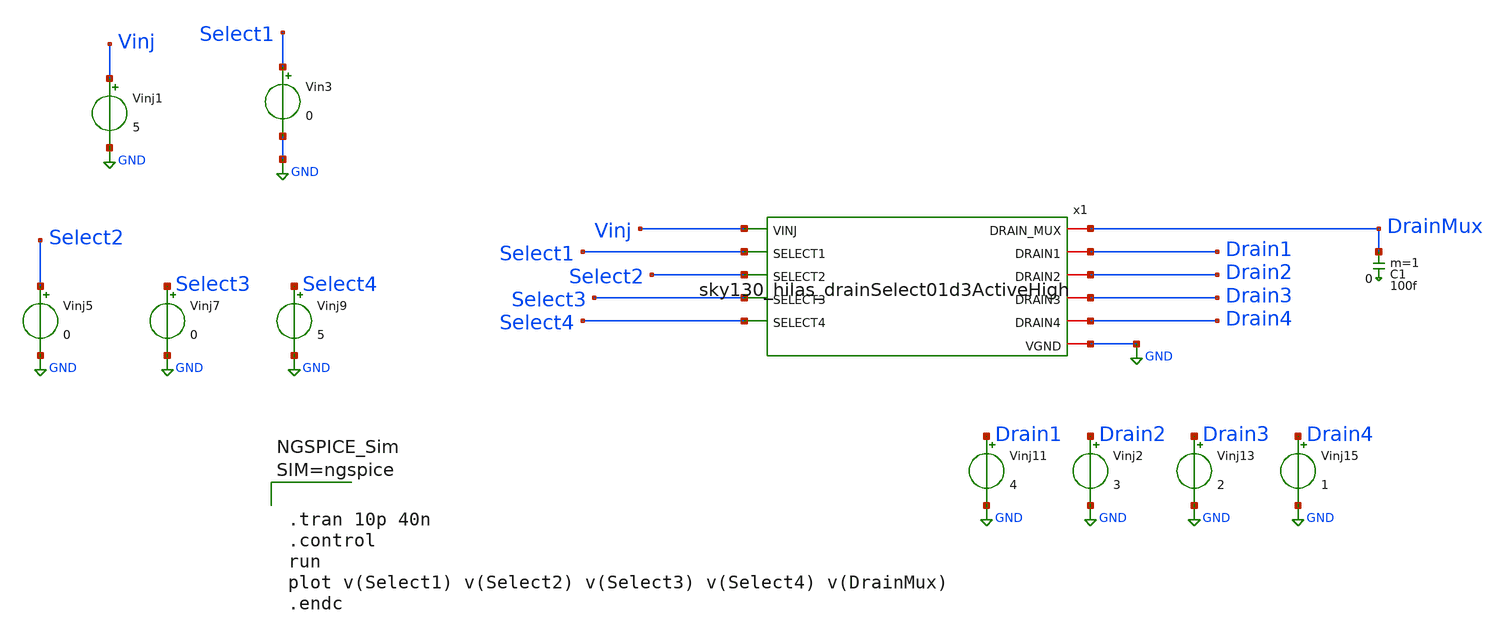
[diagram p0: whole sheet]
** sch_path: sky130_cells/Practice/DrainSelect/drainSelectActiveHighTB.sch
**.subckt drainSelectActiveHighTB
Vinj1 Vinj GND 5
Vin3 Select1 GND 0
Vinj5 Select2 GND 0
Vinj7 Select3 GND 0
Vinj9 Select4 GND 5
Vinj11 Drain1 GND 4
x1 Vinj DrainMux Select1 Drain1 Select2 Drain2 Select3 Drain3 Select4 Drain4 GND
+ sky130_hilas_drainSelect01d3ActiveHigh
C1 DrainMux 0 100f m=1
Vinj2 Drain2 GND 3
Vinj13 Drain3 GND 2
Vinj15 Drain4 GND 1
**** begin user architecture code
 .lib /usr/local/share/pdk/sky130A/libs.tech/ngspice/sky130.lib.spice tt



.tran 10p 40n
.control
run
plot v(Select1) v(Select2) v(Select3) v(Select4) v(DrainMux)
.endc



**** end user architecture code
**.ends

* expanding   symbol:  sky130_cells/Practice/DrainSelect/sky130_hilas_drainSelect01d3ActiveHigh.sym
*+ # of pins=11
** sym_path: sky130_cells/Practice/DrainSelect/sky130_hilas_drainSelect01d3ActiveHigh.sym
** sch_path: sky130_cells/Practice/DrainSelect/sky130_hilas_drainSelect01d3ActiveHigh.sch
.subckt sky130_hilas_drainSelect01d3ActiveHigh VINJ DRAIN_MUX SELECT1 DRAIN1 SELECT2 DRAIN2 SELECT3
+ DRAIN3 SELECT4 DRAIN4 VGND
*.ipin SELECT1
*.iopin DRAIN_MUX
*.iopin DRAIN1
*.ipin VINJ
*.ipin SELECT2
*.iopin DRAIN2
*.ipin SELECT3
*.iopin DRAIN3
*.ipin SELECT4
*.iopin DRAIN4
*.iopin VGND
XM15 net1 SELECT1 VGND VGND sky130_fd_pr__nfet_g5v0d10v5 L=0.5 W=1 nf=1 ad='int((nf+1)/2) * W/nf * 0.29'
+ as='int((nf+2)/2) * W/nf * 0.29' pd='2*int((nf+1)/2) * (W/nf + 0.29)' ps='2*int((nf+2)/2) * (W/nf + 0.29)'
+ nrd='0.29 / W' nrs='0.29 / W' sa=0 sb=0 sd=0 mult=1 m=1
XM17 DRAIN1 net1 DRAIN_MUX VINJ sky130_fd_pr__pfet_g5v0d10v5 L=0.5 W=1 nf=1 ad='int((nf+1)/2) * W/nf * 0.29'
+ as='int((nf+2)/2) * W/nf * 0.29' pd='2*int((nf+1)/2) * (W/nf + 0.29)' ps='2*int((nf+2)/2) * (W/nf + 0.29)'
+ nrd='0.29 / W' nrs='0.29 / W' sa=0 sb=0 sd=0 mult=1 m=1
XM30 VINJ SELECT1 DRAIN1 VINJ sky130_fd_pr__pfet_g5v0d10v5 L=0.5 W=1 nf=1 ad='int((nf+1)/2) * W/nf * 0.29'
+ as='int((nf+2)/2) * W/nf * 0.29' pd='2*int((nf+1)/2) * (W/nf + 0.29)' ps='2*int((nf+2)/2) * (W/nf + 0.29)'
+ nrd='0.29 / W' nrs='0.29 / W' sa=0 sb=0 sd=0 mult=1 m=1
XM31 net1 SELECT1 VINJ VINJ sky130_fd_pr__pfet_g5v0d10v5 L=0.5 W=1 nf=1 ad='int((nf+1)/2) * W/nf * 0.29'
+ as='int((nf+2)/2) * W/nf * 0.29' pd='2*int((nf+1)/2) * (W/nf + 0.29)' ps='2*int((nf+2)/2) * (W/nf + 0.29)'
+ nrd='0.29 / W' nrs='0.29 / W' sa=0 sb=0 sd=0 mult=1 m=1
XM35 DRAIN_MUX SELECT1 DRAIN1 VGND sky130_fd_pr__nfet_g5v0d10v5 L=0.5 W=1 nf=1 ad='int((nf+1)/2) * W/nf * 0.29'
+ as='int((nf+2)/2) * W/nf * 0.29' pd='2*int((nf+1)/2) * (W/nf + 0.29)' ps='2*int((nf+2)/2) * (W/nf + 0.29)'
+ nrd='0.29 / W' nrs='0.29 / W' sa=0 sb=0 sd=0 mult=1 m=1
XM1 net2 SELECT2 VGND VGND sky130_fd_pr__nfet_g5v0d10v5 L=0.5 W=1 nf=1 ad='int((nf+1)/2) * W/nf * 0.29'
+ as='int((nf+2)/2) * W/nf * 0.29' pd='2*int((nf+1)/2) * (W/nf + 0.29)' ps='2*int((nf+2)/2) * (W/nf + 0.29)'
+ nrd='0.29 / W' nrs='0.29 / W' sa=0 sb=0 sd=0 mult=1 m=1
XM2 DRAIN2 net2 DRAIN_MUX VINJ sky130_fd_pr__pfet_g5v0d10v5 L=0.5 W=1 nf=1 ad='int((nf+1)/2) * W/nf * 0.29'
+ as='int((nf+2)/2) * W/nf * 0.29' pd='2*int((nf+1)/2) * (W/nf + 0.29)' ps='2*int((nf+2)/2) * (W/nf + 0.29)'
+ nrd='0.29 / W' nrs='0.29 / W' sa=0 sb=0 sd=0 mult=1 m=1
XM3 VINJ SELECT2 DRAIN2 VINJ sky130_fd_pr__pfet_g5v0d10v5 L=0.5 W=1 nf=1 ad='int((nf+1)/2) * W/nf * 0.29'
+ as='int((nf+2)/2) * W/nf * 0.29' pd='2*int((nf+1)/2) * (W/nf + 0.29)' ps='2*int((nf+2)/2) * (W/nf + 0.29)'
+ nrd='0.29 / W' nrs='0.29 / W' sa=0 sb=0 sd=0 mult=1 m=1
XM4 net2 SELECT2 VINJ VINJ sky130_fd_pr__pfet_g5v0d10v5 L=0.5 W=1 nf=1 ad='int((nf+1)/2) * W/nf * 0.29'
+ as='int((nf+2)/2) * W/nf * 0.29' pd='2*int((nf+1)/2) * (W/nf + 0.29)' ps='2*int((nf+2)/2) * (W/nf + 0.29)'
+ nrd='0.29 / W' nrs='0.29 / W' sa=0 sb=0 sd=0 mult=1 m=1
XM5 DRAIN_MUX SELECT2 DRAIN2 VGND sky130_fd_pr__nfet_g5v0d10v5 L=0.5 W=1 nf=1 ad='int((nf+1)/2) * W/nf * 0.29'
+ as='int((nf+2)/2) * W/nf * 0.29' pd='2*int((nf+1)/2) * (W/nf + 0.29)' ps='2*int((nf+2)/2) * (W/nf + 0.29)'
+ nrd='0.29 / W' nrs='0.29 / W' sa=0 sb=0 sd=0 mult=1 m=1
XM6 net3 SELECT3 VGND VGND sky130_fd_pr__nfet_g5v0d10v5 L=0.5 W=1 nf=1 ad='int((nf+1)/2) * W/nf * 0.29'
+ as='int((nf+2)/2) * W/nf * 0.29' pd='2*int((nf+1)/2) * (W/nf + 0.29)' ps='2*int((nf+2)/2) * (W/nf + 0.29)'
+ nrd='0.29 / W' nrs='0.29 / W' sa=0 sb=0 sd=0 mult=1 m=1
XM7 DRAIN3 net3 DRAIN_MUX VINJ sky130_fd_pr__pfet_g5v0d10v5 L=0.5 W=1 nf=1 ad='int((nf+1)/2) * W/nf * 0.29'
+ as='int((nf+2)/2) * W/nf * 0.29' pd='2*int((nf+1)/2) * (W/nf + 0.29)' ps='2*int((nf+2)/2) * (W/nf + 0.29)'
+ nrd='0.29 / W' nrs='0.29 / W' sa=0 sb=0 sd=0 mult=1 m=1
XM8 VINJ SELECT3 DRAIN3 VINJ sky130_fd_pr__pfet_g5v0d10v5 L=0.5 W=1 nf=1 ad='int((nf+1)/2) * W/nf * 0.29'
+ as='int((nf+2)/2) * W/nf * 0.29' pd='2*int((nf+1)/2) * (W/nf + 0.29)' ps='2*int((nf+2)/2) * (W/nf + 0.29)'
+ nrd='0.29 / W' nrs='0.29 / W' sa=0 sb=0 sd=0 mult=1 m=1
XM9 net3 SELECT3 VINJ VINJ sky130_fd_pr__pfet_g5v0d10v5 L=0.5 W=1 nf=1 ad='int((nf+1)/2) * W/nf * 0.29'
+ as='int((nf+2)/2) * W/nf * 0.29' pd='2*int((nf+1)/2) * (W/nf + 0.29)' ps='2*int((nf+2)/2) * (W/nf + 0.29)'
+ nrd='0.29 / W' nrs='0.29 / W' sa=0 sb=0 sd=0 mult=1 m=1
XM10 DRAIN_MUX SELECT3 DRAIN3 VGND sky130_fd_pr__nfet_g5v0d10v5 L=0.5 W=1 nf=1 ad='int((nf+1)/2) * W/nf * 0.29'
+ as='int((nf+2)/2) * W/nf * 0.29' pd='2*int((nf+1)/2) * (W/nf + 0.29)' ps='2*int((nf+2)/2) * (W/nf + 0.29)'
+ nrd='0.29 / W' nrs='0.29 / W' sa=0 sb=0 sd=0 mult=1 m=1
XM11 net4 SELECT4 VGND VGND sky130_fd_pr__nfet_g5v0d10v5 L=0.5 W=1 nf=1 ad='int((nf+1)/2) * W/nf * 0.29'
+ as='int((nf+2)/2) * W/nf * 0.29' pd='2*int((nf+1)/2) * (W/nf + 0.29)' ps='2*int((nf+2)/2) * (W/nf + 0.29)'
+ nrd='0.29 / W' nrs='0.29 / W' sa=0 sb=0 sd=0 mult=1 m=1
XM12 DRAIN4 net4 DRAIN_MUX VINJ sky130_fd_pr__pfet_g5v0d10v5 L=0.5 W=1 nf=1 ad='int((nf+1)/2) * W/nf * 0.29'
+ as='int((nf+2)/2) * W/nf * 0.29' pd='2*int((nf+1)/2) * (W/nf + 0.29)' ps='2*int((nf+2)/2) * (W/nf + 0.29)'
+ nrd='0.29 / W' nrs='0.29 / W' sa=0 sb=0 sd=0 mult=1 m=1
XM13 VINJ SELECT4 DRAIN4 VINJ sky130_fd_pr__pfet_g5v0d10v5 L=0.5 W=1 nf=1 ad='int((nf+1)/2) * W/nf * 0.29'
+ as='int((nf+2)/2) * W/nf * 0.29' pd='2*int((nf+1)/2) * (W/nf + 0.29)' ps='2*int((nf+2)/2) * (W/nf + 0.29)'
+ nrd='0.29 / W' nrs='0.29 / W' sa=0 sb=0 sd=0 mult=1 m=1
XM14 net4 SELECT4 VINJ VINJ sky130_fd_pr__pfet_g5v0d10v5 L=0.5 W=1 nf=1 ad='int((nf+1)/2) * W/nf * 0.29'
+ as='int((nf+2)/2) * W/nf * 0.29' pd='2*int((nf+1)/2) * (W/nf + 0.29)' ps='2*int((nf+2)/2) * (W/nf + 0.29)'
+ nrd='0.29 / W' nrs='0.29 / W' sa=0 sb=0 sd=0 mult=1 m=1
XM16 DRAIN_MUX SELECT4 DRAIN4 VGND sky130_fd_pr__nfet_g5v0d10v5 L=0.5 W=1 nf=1 ad='int((nf+1)/2) * W/nf * 0.29'
+ as='int((nf+2)/2) * W/nf * 0.29' pd='2*int((nf+1)/2) * (W/nf + 0.29)' ps='2*int((nf+2)/2) * (W/nf + 0.29)'
+ nrd='0.29 / W' nrs='0.29 / W' sa=0 sb=0 sd=0 mult=1 m=1
.ends

.GLOBAL GND
.GLOBAL VGND
.end
